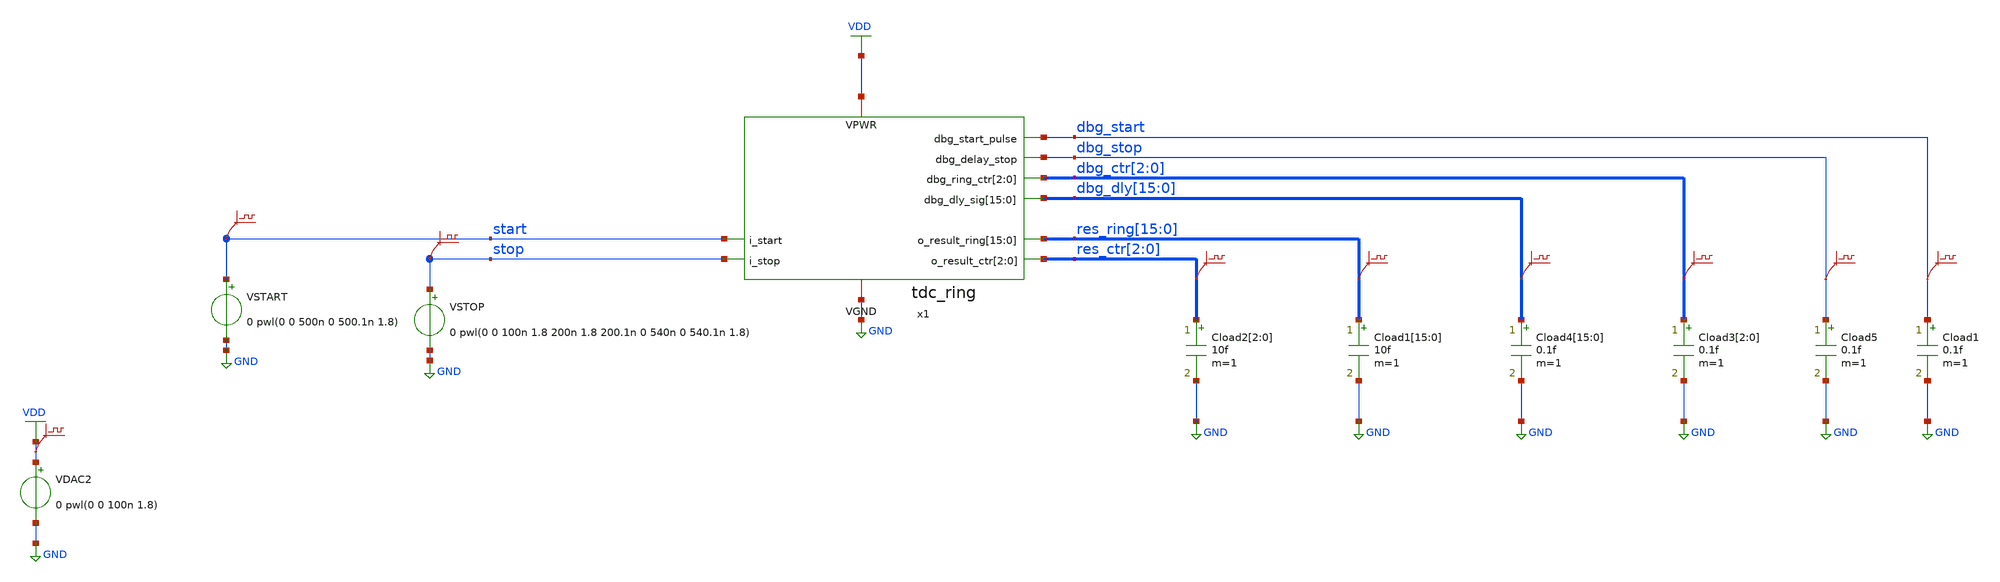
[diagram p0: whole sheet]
** sch_path: sim/tb_tt06_tdc.sch
**.subckt tb_tt06_tdc
VSTART start GND 0 pwl(0 0 500n 0 500.1n 1.8)
.save v(start)
VSTOP stop GND 0 pwl(0 0 100n 1.8 200n 1.8 200.1n 0 540n 0 540.1n 1.8)
.save v(stop)
Cload1[15] res_ring[15] GND 10f m=1
Cload1[14] res_ring[14] GND 10f m=1
Cload1[13] res_ring[13] GND 10f m=1
Cload1[12] res_ring[12] GND 10f m=1
Cload1[11] res_ring[11] GND 10f m=1
Cload1[10] res_ring[10] GND 10f m=1
Cload1[9] res_ring[9] GND 10f m=1
Cload1[8] res_ring[8] GND 10f m=1
Cload1[7] res_ring[7] GND 10f m=1
Cload1[6] res_ring[6] GND 10f m=1
Cload1[5] res_ring[5] GND 10f m=1
Cload1[4] res_ring[4] GND 10f m=1
Cload1[3] res_ring[3] GND 10f m=1
Cload1[2] res_ring[2] GND 10f m=1
Cload1[1] res_ring[1] GND 10f m=1
Cload1[0] res_ring[0] GND 10f m=1
.save v(res_ring[15])
.save v(res_ring[14])
.save v(res_ring[13])
.save v(res_ring[12])
.save v(res_ring[11])
.save v(res_ring[10])
.save v(res_ring[9])
.save v(res_ring[8])
.save v(res_ring[7])
.save v(res_ring[6])
.save v(res_ring[5])
.save v(res_ring[4])
.save v(res_ring[3])
.save v(res_ring[2])
.save v(res_ring[1])
.save v(res_ring[0])
.save v(vdd)
VDAC2 VDD GND 0 pwl(0 0 100n 1.8)
Cload2[2] res_ctr[2] GND 10f m=1
Cload2[1] res_ctr[1] GND 10f m=1
Cload2[0] res_ctr[0] GND 10f m=1
.save v(res_ctr[2])
.save v(res_ctr[1])
.save v(res_ctr[0])
x1 start stop res_ring[15] res_ring[14] res_ring[13] res_ring[12] res_ring[11] res_ring[10]
+ res_ring[9] res_ring[8] res_ring[7] res_ring[6] res_ring[5] res_ring[4] res_ring[3] res_ring[2] res_ring[1]
+ res_ring[0] res_ctr[2] res_ctr[1] res_ctr[0] dbg_start dbg_stop dbg_ctr[2] dbg_ctr[1] dbg_ctr[0] dbg_dly[15]
+ dbg_dly[14] dbg_dly[13] dbg_dly[12] dbg_dly[11] dbg_dly[10] dbg_dly[9] dbg_dly[8] dbg_dly[7] dbg_dly[6]
+ dbg_dly[5] dbg_dly[4] dbg_dly[3] dbg_dly[2] dbg_dly[1] dbg_dly[0] VDD GND tdc_ring
Cload3[2] dbg_ctr[2] GND 0.1f m=1
Cload3[1] dbg_ctr[1] GND 0.1f m=1
Cload3[0] dbg_ctr[0] GND 0.1f m=1
Cload4[15] dbg_dly[15] GND 0.1f m=1
Cload4[14] dbg_dly[14] GND 0.1f m=1
Cload4[13] dbg_dly[13] GND 0.1f m=1
Cload4[12] dbg_dly[12] GND 0.1f m=1
Cload4[11] dbg_dly[11] GND 0.1f m=1
Cload4[10] dbg_dly[10] GND 0.1f m=1
Cload4[9] dbg_dly[9] GND 0.1f m=1
Cload4[8] dbg_dly[8] GND 0.1f m=1
Cload4[7] dbg_dly[7] GND 0.1f m=1
Cload4[6] dbg_dly[6] GND 0.1f m=1
Cload4[5] dbg_dly[5] GND 0.1f m=1
Cload4[4] dbg_dly[4] GND 0.1f m=1
Cload4[3] dbg_dly[3] GND 0.1f m=1
Cload4[2] dbg_dly[2] GND 0.1f m=1
Cload4[1] dbg_dly[1] GND 0.1f m=1
Cload4[0] dbg_dly[0] GND 0.1f m=1
.save v(dbg_dly[15])
.save v(dbg_dly[14])
.save v(dbg_dly[13])
.save v(dbg_dly[12])
.save v(dbg_dly[11])
.save v(dbg_dly[10])
.save v(dbg_dly[9])
.save v(dbg_dly[8])
.save v(dbg_dly[7])
.save v(dbg_dly[6])
.save v(dbg_dly[5])
.save v(dbg_dly[4])
.save v(dbg_dly[3])
.save v(dbg_dly[2])
.save v(dbg_dly[1])
.save v(dbg_dly[0])
.save v(dbg_ctr[2])
.save v(dbg_ctr[1])
.save v(dbg_ctr[0])
Cload5 dbg_stop GND 0.1f m=1
Cload1 dbg_start GND 0.1f m=1
.save v(dbg_stop)
.save v(dbg_start)
**** begin user architecture code



* ngspice commands
****************

****************
* Misc
****************
.param fclk=10MEG
.options method=gear maxord=2
.temp 30

.control
set num_threads=6
tran 0.01n 600n

write tb_tt06_tdc.raw

*exit
.endc




** opencircuitdesign pdks install
.lib $::SKYWATER_MODELS/sky130.lib.spice tt


**** end user architecture code
**.ends

* expanding   symbol:  /foss/designs/sim/tdc_ring.sym # of pins=10
** sym_path: sim/tdc_ring.sym
.include tdc_ring.pex.spice
.GLOBAL VDD
.GLOBAL GND
.end
